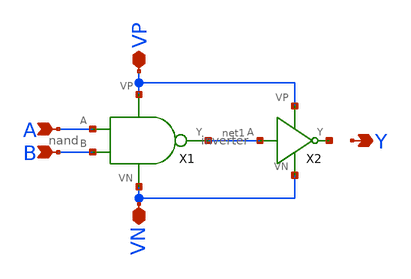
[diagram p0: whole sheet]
** sch_path: mp1/and.sch
**.subckt and A B VP VN Y
*.ipin A
*.ipin B
*.iopin VP
*.iopin VN
*.opin Y
X1 A B net1 VP VN nand
X2 net1 net2 VP VN inverter
**.ends

* expanding   symbol:  /home/madvlsi/madvlsi/mp1/nand.sym # of pins=5
** sym_path: mp1/nand.sym
** sch_path: mp1/nand.sch
.subckt nand A B Y VP VN
*.ipin A
*.opin Y
*.iopin VP
*.iopin VN
*.ipin B
XM1 Y A VP VP sky130_fd_pr__pfet_01v8 L=0.15 W=1 nf=1 ad='int((nf+1)/2) * W/nf * 0.29' as='int((nf+2)/2) * W/nf * 0.29'
+ pd='2*int((nf+1)/2) * (W/nf + 0.29)' ps='2*int((nf+2)/2) * (W/nf + 0.29)' nrd='0.29 / W' nrs='0.29 / W'
+ sa=0 sb=0 sd=0 mult=1 m=1
XM2 Y B VP VP sky130_fd_pr__pfet_01v8 L=0.15 W=1 nf=1 ad='int((nf+1)/2) * W/nf * 0.29' as='int((nf+2)/2) * W/nf * 0.29'
+ pd='2*int((nf+1)/2) * (W/nf + 0.29)' ps='2*int((nf+2)/2) * (W/nf + 0.29)' nrd='0.29 / W' nrs='0.29 / W'
+ sa=0 sb=0 sd=0 mult=1 m=1
XM3 Y A net1 Y sky130_fd_pr__nfet_01v8 L=0.15 W=1 nf=1 ad='int((nf+1)/2) * W/nf * 0.29' as='int((nf+2)/2) * W/nf * 0.29'
+ pd='2*int((nf+1)/2) * (W/nf + 0.29)' ps='2*int((nf+2)/2) * (W/nf + 0.29)' nrd='0.29 / W' nrs='0.29 / W'
+ sa=0 sb=0 sd=0 mult=1 m=1
XM4 net1 B VN net1 sky130_fd_pr__nfet_01v8 L=0.15 W=1 nf=1 ad='int((nf+1)/2) * W/nf * 0.29' as='int((nf+2)/2) * W/nf * 0.29'
+ pd='2*int((nf+1)/2) * (W/nf + 0.29)' ps='2*int((nf+2)/2) * (W/nf + 0.29)' nrd='0.29 / W' nrs='0.29 / W'
+ sa=0 sb=0 sd=0 mult=1 m=1
.ends


* expanding   symbol:  /home/madvlsi/madvlsi/mp1/inverter.sym # of pins=4
** sym_path: /home/madvlsi/madvlsi/mp1/inverter.sym
** sch_path: /home/madvlsi/madvlsi/mp1/inverter.sch
.subckt inverter A Y VP VN
*.ipin A
*.iopin VP
*.iopin VN
*.opin Y
XM1 Y A VN VN sky130_fd_pr__nfet_01v8 L=0.15 W=1 nf=1 ad='int((nf+1)/2) * W/nf * 0.29' as='int((nf+2)/2) * W/nf * 0.29'
+ pd='2*int((nf+1)/2) * (W/nf + 0.29)' ps='2*int((nf+2)/2) * (W/nf + 0.29)' nrd='0.29 / W' nrs='0.29 / W'
+ sa=0 sb=0 sd=0 mult=1 m=1
XM2 Y A VP VP sky130_fd_pr__pfet_01v8 L=0.15 W=1 nf=1 ad='int((nf+1)/2) * W/nf * 0.29' as='int((nf+2)/2) * W/nf * 0.29'
+ pd='2*int((nf+1)/2) * (W/nf + 0.29)' ps='2*int((nf+2)/2) * (W/nf + 0.29)' nrd='0.29 / W' nrs='0.29 / W'
+ sa=0 sb=0 sd=0 mult=1 m=1
.ends

.end
